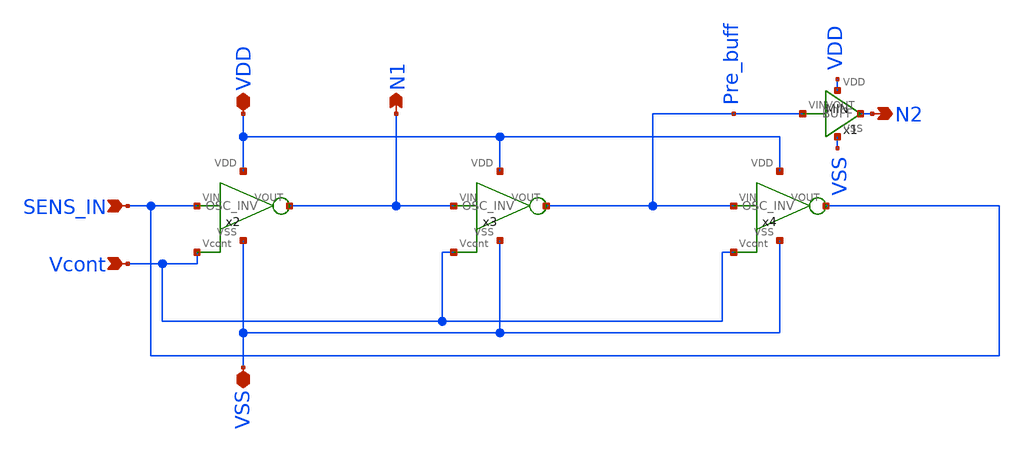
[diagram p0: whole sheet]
** sch_path: ABC123_SDC/design_data/klayout/OSC/OSC_RING/OSC_RING.sch
**.subckt OSC_RING SENS_IN VDD VSS N1 N2 Vcont
*.ipin SENS_IN
*.iopin VDD
*.iopin VSS
*.opin N1
*.opin N2
*.ipin Vcont
x2 VDD SENS_IN N1 VSS Vcont OSC_INV
x3 VDD N1 Pre_buff VSS Vcont OSC_INV
x4 VDD Pre_buff SENS_IN VSS Vcont OSC_INV
x1 Pre_buff N2 VDD VSS BUFF
**.ends
.end
